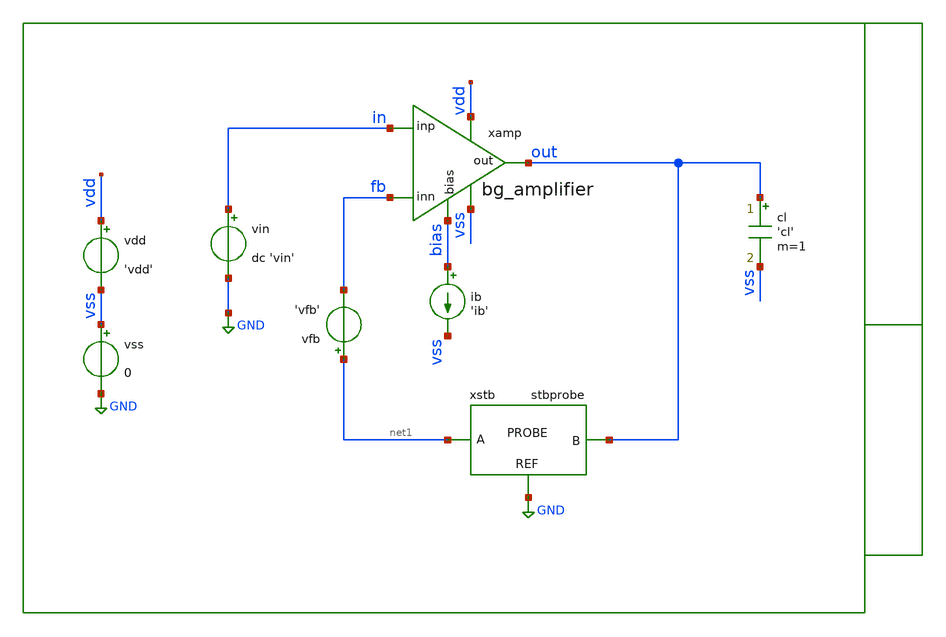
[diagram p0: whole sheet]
** sch_path: xschem/tb/bandgap_cm/bg_amplifier/ac_bg_amplifier_stb.sch
**.subckt ac_bg_amplifier_stb
vin in GND dc 'vin'
cl out vss 'cl' m=1
vdd vdd vss 'vdd'
vss vss GND 0
xamp vdd out in fb vss bias bg_amplifier
ib bias vss 'ib'
xstb net1 out GND stbprobe
vfb net1 fb 'vfb'
**** begin user architecture code

* Control

.param vdd=3.3

* emulate bandgap setup
.param vfb=1.4
.param vin=0.7
.param ib=1u
.param cl=1p

.temp 27

.control

let runs=2
let run=0

alter v.xstb.vprobe1 acmag=1
alter i.xstb.iprobe1 acmag=0

dowhile run < runs
set run ="$&run"

ac dec 100 0.01 10G

alter v.xstb.vprobe1 acmag=0
alter i.xstb.iprobe1 acmag=1

let run = run + 1

end

let ip11 = ac1.i(v.xstb.vprobe1)
let ip12 = ac1.i(v.xstb.vprobe2)
let ip21 = ac2.i(v.xstb.vprobe1)
let ip22 = ac2.i(v.xstb.vprobe2)
let vprb1 = ac1.v(xstb.probe)
let vprb2 = ac2.v(xstb.probe)

let av = 1/(1/(2*(ip11*vprb2-vprb1*ip21)+vprb1+ip21)-1)

let phase=180/PI*cph(av)

gnuplot p1 vdb(av)
gnuplot p2 phase

meas ac gain find vdb(av) at=0.01
meas ac ugbw when vdb(av)=0
meas ac pm_pha find phase when vdb(av)=0

let pm = 180 + pm_pha
print gain
print ugbw
print pm

set wr_singlescale
set wr_vecnames
wrdata data.csv vdb(av) phase

.endc


 * Model Corners

.include $::CORNERS/ngspice/tt.spice
*.include $::CORNERS/ngspice/ff.spice
*.include $::CORNERS/ngspice/ss.spice
*.include $::CORNERS/ngspice/sf.spice
*.include $::CORNERS/ngspice/fs.spice

 * extract

* pex
*.include $::DESIGN_PATH/sch/bandgap_cm/bg_amplifier/bg_amplifier.pex.spice

**** end user architecture code
**.ends

* expanding   symbol:  sch/bandgap_cm/bg_amplifier/bg_amplifier.sym # of pins=6
** sym_path: xschem/sch/bandgap_cm/bg_amplifier/bg_amplifier.sym
** sch_path: xschem/sch/bandgap_cm/bg_amplifier/bg_amplifier.sch
.subckt bg_amplifier vdd out inp inn vss bias
*.ipin inn
*.ipin inp
*.opin out
*.iopin bias
*.iopin vdd
*.iopin vss
XMB5 vbn1 vbn1 vss vss nfet_06v0 L=2u W=16u nf=2 ad='int((nf+1)/2) * W/nf * 0.18u' as='int((nf+2)/2) * W/nf * 0.18u'
+ pd='2*int((nf+1)/2) * (W/nf + 0.18u)' ps='2*int((nf+2)/2) * (W/nf + 0.18u)' nrd='0.18u / W' nrs='0.18u / W'
+ sa=0 sb=0 sd=0 m=4 par=4
XMC1 von vbn1 vss vss nfet_06v0 L=2u W=16u nf=2 ad='int((nf+1)/2) * W/nf * 0.18u' as='int((nf+2)/2) * W/nf * 0.18u'
+ pd='2*int((nf+1)/2) * (W/nf + 0.18u)' ps='2*int((nf+2)/2) * (W/nf + 0.18u)' nrd='0.18u / W' nrs='0.18u / W'
+ sa=0 sb=0 sd=0 m=10 par=10
XMC2 vop vbn1 vss vss nfet_06v0 L=2u W=16u nf=2 ad='int((nf+1)/2) * W/nf * 0.18u' as='int((nf+2)/2) * W/nf * 0.18u'
+ pd='2*int((nf+1)/2) * (W/nf + 0.18u)' ps='2*int((nf+2)/2) * (W/nf + 0.18u)' nrd='0.18u / W' nrs='0.18u / W'
+ sa=0 sb=0 sd=0 m=10 par=10
XMC3 mirr vbn2 von vss nfet_06v0 L=2u W=16u nf=2 ad='int((nf+1)/2) * W/nf * 0.18u' as='int((nf+2)/2) * W/nf * 0.18u'
+ pd='2*int((nf+1)/2) * (W/nf + 0.18u)' ps='2*int((nf+2)/2) * (W/nf + 0.18u)' nrd='0.18u / W' nrs='0.18u / W'
+ sa=0 sb=0 sd=0 m=4 par=4
XMC4 out vbn2 vop vss nfet_06v0 L=2u W=16u nf=2 ad='int((nf+1)/2) * W/nf * 0.18u' as='int((nf+2)/2) * W/nf * 0.18u'
+ pd='2*int((nf+1)/2) * (W/nf + 0.18u)' ps='2*int((nf+2)/2) * (W/nf + 0.18u)' nrd='0.18u / W' nrs='0.18u / W'
+ sa=0 sb=0 sd=0 m=4 par=4
XMB3 bias bias vbp1 vdd pfet_06v0 L=2u W=16u nf=2 ad='int((nf+1)/2) * W/nf * 0.18u' as='int((nf+2)/2) * W/nf * 0.18u'
+ pd='2*int((nf+1)/2) * (W/nf + 0.18u)' ps='2*int((nf+2)/2) * (W/nf + 0.18u)' nrd='0.18u / W' nrs='0.18u / W'
+ sa=0 sb=0 sd=0 m=2 par=2
XMB1 vbp1 vbp1 vdd vdd pfet_06v0 L=2u W=16u nf=2 ad='int((nf+1)/2) * W/nf * 0.18u' as='int((nf+2)/2) * W/nf * 0.18u'
+ pd='2*int((nf+1)/2) * (W/nf + 0.18u)' ps='2*int((nf+2)/2) * (W/nf + 0.18u)' nrd='0.18u / W' nrs='0.18u / W'
+ sa=0 sb=0 sd=0 m=4 par=4
XMB2 vbn2 vbp1 vdd vdd pfet_06v0 L=2u W=16u nf=2 ad='int((nf+1)/2) * W/nf * 0.18u' as='int((nf+2)/2) * W/nf * 0.18u'
+ pd='2*int((nf+1)/2) * (W/nf + 0.18u)' ps='2*int((nf+2)/2) * (W/nf + 0.18u)' nrd='0.18u / W' nrs='0.18u / W'
+ sa=0 sb=0 sd=0 m=4 par=4
XMT1 vcm vbp1 vdd vdd pfet_06v0 L=2u W=16u nf=2 ad='int((nf+1)/2) * W/nf * 0.18u' as='int((nf+2)/2) * W/nf * 0.18u'
+ pd='2*int((nf+1)/2) * (W/nf + 0.18u)' ps='2*int((nf+2)/2) * (W/nf + 0.18u)' nrd='0.18u / W' nrs='0.18u / W'
+ sa=0 sb=0 sd=0 m=8 par=8
XMD1 von inp vcm vdd pfet_06v0 L=4u W=16u nf=2 ad='int((nf+1)/2) * W/nf * 0.18u' as='int((nf+2)/2) * W/nf * 0.18u'
+ pd='2*int((nf+1)/2) * (W/nf + 0.18u)' ps='2*int((nf+2)/2) * (W/nf + 0.18u)' nrd='0.18u / W' nrs='0.18u / W'
+ sa=0 sb=0 sd=0 m=4 par=4
XMD2 vop inn vcm vdd pfet_06v0 L=4u W=16u nf=2 ad='int((nf+1)/2) * W/nf * 0.18u' as='int((nf+2)/2) * W/nf * 0.18u'
+ pd='2*int((nf+1)/2) * (W/nf + 0.18u)' ps='2*int((nf+2)/2) * (W/nf + 0.18u)' nrd='0.18u / W' nrs='0.18u / W'
+ sa=0 sb=0 sd=0 m=4 par=4
XMC7 vda mirr vdd vdd pfet_06v0 L=2u W=16u nf=2 ad='int((nf+1)/2) * W/nf * 0.18u' as='int((nf+2)/2) * W/nf * 0.18u'
+ pd='2*int((nf+1)/2) * (W/nf + 0.18u)' ps='2*int((nf+2)/2) * (W/nf + 0.18u)' nrd='0.18u / W' nrs='0.18u / W'
+ sa=0 sb=0 sd=0 m=2 par=2
XMC8 vdb mirr vdd vdd pfet_06v0 L=2u W=16u nf=2 ad='int((nf+1)/2) * W/nf * 0.18u' as='int((nf+2)/2) * W/nf * 0.18u'
+ pd='2*int((nf+1)/2) * (W/nf + 0.18u)' ps='2*int((nf+2)/2) * (W/nf + 0.18u)' nrd='0.18u / W' nrs='0.18u / W'
+ sa=0 sb=0 sd=0 m=2 par=2
XMC5 mirr bias vda vdd pfet_06v0 L=2u W=16u nf=2 ad='int((nf+1)/2) * W/nf * 0.18u' as='int((nf+2)/2) * W/nf * 0.18u'
+ pd='2*int((nf+1)/2) * (W/nf + 0.18u)' ps='2*int((nf+2)/2) * (W/nf + 0.18u)' nrd='0.18u / W' nrs='0.18u / W'
+ sa=0 sb=0 sd=0 m=4 par=4
XMC6 out bias vdb vdd pfet_06v0 L=2u W=16u nf=2 ad='int((nf+1)/2) * W/nf * 0.18u' as='int((nf+2)/2) * W/nf * 0.18u'
+ pd='2*int((nf+1)/2) * (W/nf + 0.18u)' ps='2*int((nf+2)/2) * (W/nf + 0.18u)' nrd='0.18u / W' nrs='0.18u / W'
+ sa=0 sb=0 sd=0 m=4 par=4
XMB4 vbn2 vbn2 vbn1 vss nfet_06v0 L=2u W=16u nf=2 ad='int((nf+1)/2) * W/nf * 0.18u' as='int((nf+2)/2) * W/nf * 0.18u'
+ pd='2*int((nf+1)/2) * (W/nf + 0.18u)' ps='2*int((nf+2)/2) * (W/nf + 0.18u)' nrd='0.18u / W' nrs='0.18u / W'
+ sa=0 sb=0 sd=0 m=4 par=4
XMDUM1 vdd vdd vdd vdd pfet_06v0 L=2u W=16u nf=2 ad='int((nf+1)/2) * W/nf * 0.18u' as='int((nf+2)/2) * W/nf * 0.18u'
+ pd='2*int((nf+1)/2) * (W/nf + 0.18u)' ps='2*int((nf+2)/2) * (W/nf + 0.18u)' nrd='0.18u / W' nrs='0.18u / W'
+ sa=0 sb=0 sd=0 m=4 par=4
XMDUM2 vdd vdd vdd vdd pfet_06v0 L=2u W=16u nf=2 ad='int((nf+1)/2) * W/nf * 0.18u' as='int((nf+2)/2) * W/nf * 0.18u'
+ pd='2*int((nf+1)/2) * (W/nf + 0.18u)' ps='2*int((nf+2)/2) * (W/nf + 0.18u)' nrd='0.18u / W' nrs='0.18u / W'
+ sa=0 sb=0 sd=0 m=4 par=4
XMDUM3 vdd vdd vdd vdd pfet_06v0 L=2u W=16u nf=2 ad='int((nf+1)/2) * W/nf * 0.18u' as='int((nf+2)/2) * W/nf * 0.18u'
+ pd='2*int((nf+1)/2) * (W/nf + 0.18u)' ps='2*int((nf+2)/2) * (W/nf + 0.18u)' nrd='0.18u / W' nrs='0.18u / W'
+ sa=0 sb=0 sd=0 m=2 par=2
XMDUM4 vss vss vss vss nfet_06v0 L=2u W=16u nf=2 ad='int((nf+1)/2) * W/nf * 0.18u' as='int((nf+2)/2) * W/nf * 0.18u'
+ pd='2*int((nf+1)/2) * (W/nf + 0.18u)' ps='2*int((nf+2)/2) * (W/nf + 0.18u)' nrd='0.18u / W' nrs='0.18u / W'
+ sa=0 sb=0 sd=0 m=2 par=2
XMDUM5 vss vss vss vss nfet_06v0 L=2u W=16u nf=2 ad='int((nf+1)/2) * W/nf * 0.18u' as='int((nf+2)/2) * W/nf * 0.18u'
+ pd='2*int((nf+1)/2) * (W/nf + 0.18u)' ps='2*int((nf+2)/2) * (W/nf + 0.18u)' nrd='0.18u / W' nrs='0.18u / W'
+ sa=0 sb=0 sd=0 m=2 par=2
XMDUM6 vdd vdd vdd vdd pfet_06v0 L=4u W=16u nf=2 ad='int((nf+1)/2) * W/nf * 0.18u' as='int((nf+2)/2) * W/nf * 0.18u'
+ pd='2*int((nf+1)/2) * (W/nf + 0.18u)' ps='2*int((nf+2)/2) * (W/nf + 0.18u)' nrd='0.18u / W' nrs='0.18u / W'
+ sa=0 sb=0 sd=0 m=16 par=16
.ends


* expanding   symbol:  xschem/ideal/stbprobe/stbprobe.sym # of pins=3
** sym_path: xschem/xschem/ideal/stbprobe/stbprobe.sym
** sch_path: xschem/xschem/ideal/stbprobe/stbprobe.sch
.subckt stbprobe A B REF
*.iopin A
*.iopin B
*.iopin REF
Vprobe1 probe A 0
Iprobe1 REF probe 0
Vprobe2 probe B 0
**** begin user architecture code



**** end user architecture code
.ends

.GLOBAL GND
.end
